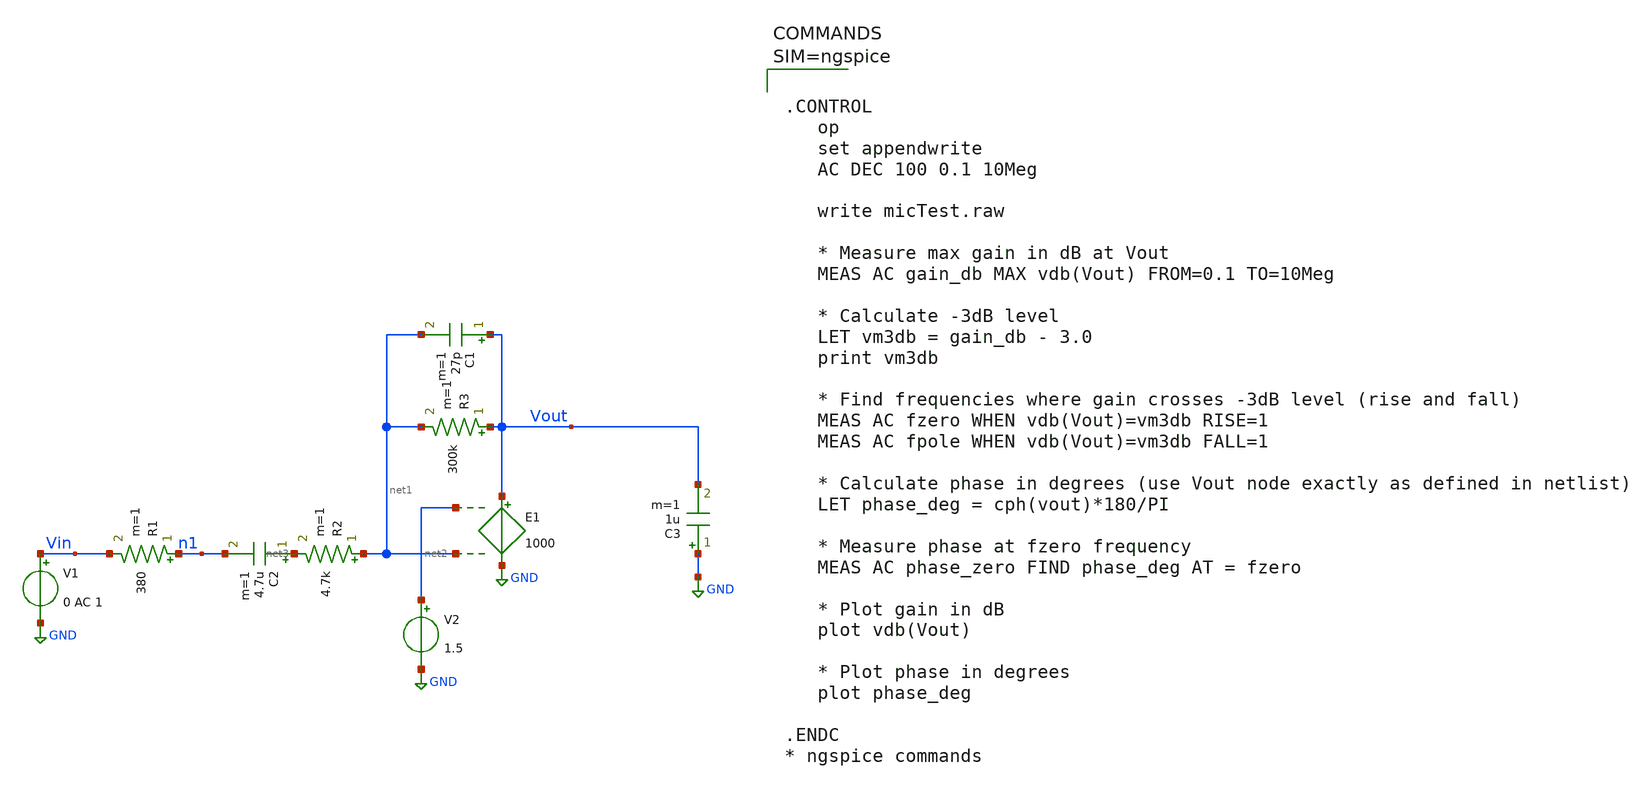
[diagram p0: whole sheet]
** sch_path: xschem/micTest.sch
**.subckt micTest
V1 Vin GND 0 AC 1
R1 n1 Vin 380 m=1
R2 net1 net3 4.7k m=1
C2 net3 n1 4.7u m=1
E1 Vout GND net2 net1 1000
R3 Vout net1 300k m=1
C1 Vout net1 27p m=1
C3 GND Vout 1u m=1
V2 net2 GND 1.5
**** begin user architecture code



.CONTROL
   op
   set appendwrite
   AC DEC 100 0.1 10Meg

   write micTest.raw

   * Measure max gain in dB at Vout
   MEAS AC gain_db MAX vdb(Vout) FROM=0.1 TO=10Meg

   * Calculate -3dB level
   LET vm3db = gain_db - 3.0
   print vm3db

   * Find frequencies where gain crosses -3dB level (rise and fall)
   MEAS AC fzero WHEN vdb(Vout)=vm3db RISE=1
   MEAS AC fpole WHEN vdb(Vout)=vm3db FALL=1

   * Calculate phase in degrees (use Vout node exactly as defined in netlist)
   LET phase_deg = cph(vout)*180/PI

   * Measure phase at fzero frequency
   MEAS AC phase_zero FIND phase_deg AT = fzero

   * Plot gain in dB
   plot vdb(Vout)

   * Plot phase in degrees
   plot phase_deg

.ENDC
* ngspice commands


**** end user architecture code
**.ends
.GLOBAL GND
.end
